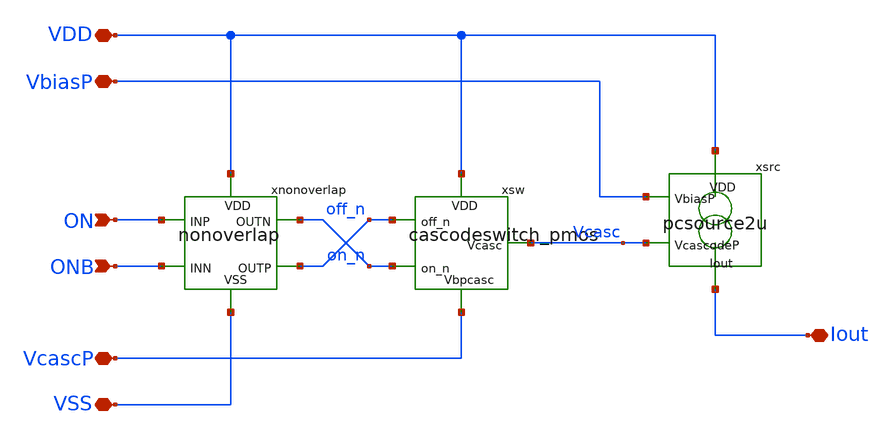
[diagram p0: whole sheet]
** sch_path: xschem/unitsource2u.sch
**.subckt unitsource2u VSS VDD VbiasP VcascP ON ONB Iout
*.iopin VSS
*.iopin VDD
*.iopin VbiasP
*.iopin VcascP
*.ipin ON
*.ipin ONB
*.iopin Iout
xnonoverlap VDD VSS ON ONB on_n off_n nonoverlap
xsw VDD off_n Vcasc on_n VcascP cascodeswitch_pmos
xsrc VDD VbiasP Vcasc Iout pcsource2u
**.ends

* expanding   symbol:  nonoverlap.sym # of pins=6
** sym_path: xschem/nonoverlap.sym
** sch_path: xschem/nonoverlap.sch
.subckt nonoverlap VDD VSS INP INN OUTN OUTP
*.iopin VSS
*.iopin VDD
*.ipin INP
*.ipin INN
*.opin OUTP
*.opin OUTN
XM1 OUTN INP VDD VDD sg13_lv_pmos w=0.3u l=0.13u ng=1 m=1 mm_ok=1
XM2 OUTP INN VDD VDD sg13_lv_pmos w=0.3u l=0.13u ng=1 m=1 mm_ok=1
XM3 OUTN OUTP VSS VSS sg13_lv_nmos w=0.15u l=0.52u ng=1 m=1 mm_ok=1
XM4 OUTP OUTN VSS VSS sg13_lv_nmos w=0.15u l=0.52u ng=1 m=1 mm_ok=1
.ends


* expanding   symbol:  cascodeswitch_pmos.sym # of pins=5
** sym_path: xschem/cascodeswitch_pmos.sym
** sch_path: xschem/cascodeswitch_pmos.sch
.subckt cascodeswitch_pmos VDD off_n Vcasc on_n Vbpcasc
*.ipin off_n
*.ipin Vbpcasc
*.opin Vcasc
*.ipin on_n
*.ipin VDD
XMpullup Vcasc off_n VDD VDD sg13_lv_pmos w=0.3u l=0.13u ng=1 m=1 mm_ok=1
XMbias Vbpcasc on_n Vcasc VDD sg13_lv_pmos w=0.3u l=0.13u ng=1 m=1 mm_ok=1
.ends


* expanding   symbol:  pcsource2u.sym # of pins=4
** sym_path: xschem/pcsource2u.sym
** sch_path: xschem/pcsource2u.sch
.subckt pcsource2u VDD VbiasP VcascodeP Iout
*.ipin VcascodeP
*.ipin VbiasP
*.opin Iout
*.ipin VDD
XMsrc drain net4 VDD net1 sg13_lv_pmos w=1.45u l=5u ng=1 m=1 mm_ok=1
XMcasc Iout net3 drain net2 sg13_lv_pmos w=1.2u l=0.6u ng=1 m=1 mm_ok=1
Vgsrc net4 VbiasP 0
.save i(vgsrc)
Vgcasc net3 VcascodeP 0
.save i(vgcasc)
Vbsrc VDD net1 0
.save i(vbsrc)
Vbcasc VDD net2 0
.save i(vbcasc)
.ends

.end
